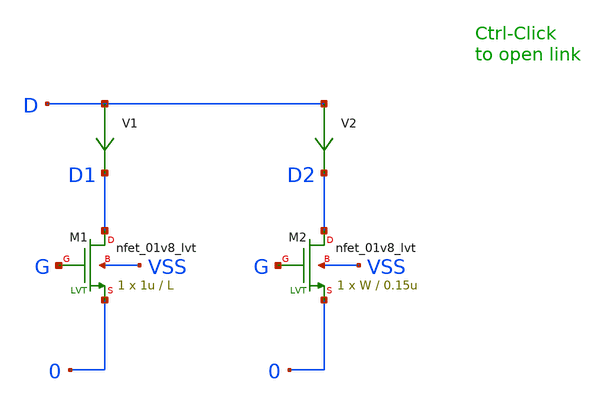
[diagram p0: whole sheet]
** sch_path: sky130_tests_ng/test_nmos_sizes.sch
* Copyright 2020 Stefan Frederik Schippers
* Licensed under the Apache License, Version 2.0 (the "License");
* you may not use this file except in compliance with the License.
* You may obtain a copy of the License at
* https://www.apache.org/licenses/LICENSE-2.0
* Unless required by applicable law or agreed to in writing, software
* distributed under the License is distributed on an "AS IS" BASIS,
* WITHOUT WARRANTIES OR CONDITIONS OF ANY KIND, either express or implied.
* See the License for the specific language governing permissions and
* limitations under the License.
**.subckt test_nmos_sizes
XM1 D1 G 0 VSS sky130_fd_pr__nfet_01v8_lvt w=1u l=L ad='w * 0.29u' pd='2 * (w + 0.29u)' as='w * 0.29u'
+ ps='2 * (w + 0.29u)' nrd='0.29u / w' nrs='0.29u / w' sa=0 sb=0 sd=0 nf=1 mult=1 m=1
XM2 D2 G 0 VSS sky130_fd_pr__nfet_01v8_lvt w=W l=0.15u ad='w * 0.29u' pd='2 * (w + 0.29u)' as='w * 0.29u'
+ ps='2 * (w + 0.29u)' nrd='0.29u / w' nrs='0.29u / w' sa=0 sb=0 sd=0 nf=1 mult=1 m=1
V2 D D2 0
.save i(v2)
V1 D D1 0
.save i(v1)
**** begin user architecture code

**** end user architecture code
**.ends
**** begin user architecture code

* .option SCALE=1e-6
.option method=gear seed=12
.param l=0.15u
.param w=0.5u

vd d 0 0
vg g 0 0
.control
dc vd 0 2 0.01 vg 0 2 0.2
alterparam l=0.18u
alterparam w=1u
reset
dc vd 0 2 0.01 vg 0 2 0.2
alterparam l=0.3u
alterparam w=2u
reset
dc vd 0 2 0.01 vg 0 2 0.2
alterparam l=0.5u
alterparam w=3u
reset
dc vd 0 2 0.01 vg 0 2 0.2

.endc





**** end user architecture code
.end
